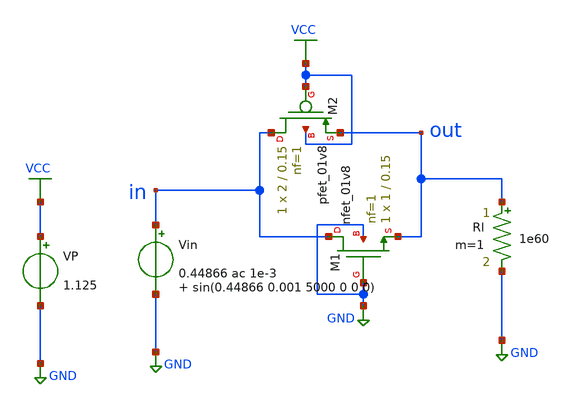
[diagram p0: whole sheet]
** sch_path: Amplifier_Inv/xschem/tb_res.sch
**.subckt tb_res
XM1 in GND out GND sky130_fd_pr__nfet_01v8 L=0.15 W=1 nf=1 ad='int((nf+1)/2) * W/nf * 0.29' as='int((nf+2)/2) * W/nf * 0.29'
+ pd='2*int((nf+1)/2) * (W/nf + 0.29)' ps='2*int((nf+2)/2) * (W/nf + 0.29)' nrd='0.29 / W' nrs='0.29 / W'
+ sa=0 sb=0 sd=0 mult=1 m=1
XM2 in VCC out VCC sky130_fd_pr__pfet_01v8 L=0.15 W=2 nf=1 ad='int((nf+1)/2) * W/nf * 0.29' as='int((nf+2)/2) * W/nf * 0.29'
+ pd='2*int((nf+1)/2) * (W/nf + 0.29)' ps='2*int((nf+2)/2) * (W/nf + 0.29)' nrd='0.29 / W' nrs='0.29 / W'
+ sa=0 sb=0 sd=0 mult=1 m=1
VP VCC GND 1.125
Vin in GND 0.44866 ac 1e-3 sin(0.44866 0.001 5000 0 0 0)
Rl out GND 1e60 m=1
**** begin user architecture code

** opencircuitdesign pdks install
.lib $::SKYWATER_MODELS/sky130.lib.spice tt



.control

  dc Vin 0 1 0.00001
  save all
  let r = (v(out)-v(in))/i(Vin)
  write tb_inv_sky130_a_noise_res_DC_v2.raw r v(in)

.endc


**** end user architecture code
**.ends
.GLOBAL GND
.GLOBAL VCC
.end
